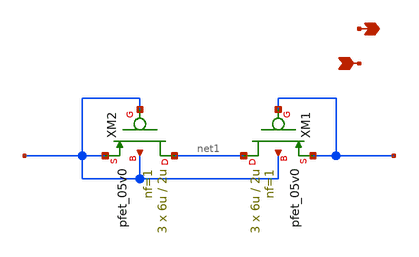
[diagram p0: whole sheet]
** sch_path: design/schematics/CCIA/CCIA/Resistors/NS_cic_bms_inst_amp_pseudo_res.sch
**.subckt NS_cic_bms_inst_amp_pseudo_res - +
*.opin -
*.ipin +
XM1 net1 - - + pfet_05v0 L=2u W=6u nf=1 ad='int((nf+1)/2) * W/nf * 0.18u' as='int((nf+2)/2) * W/nf * 0.18u'
+ pd='2*int((nf+1)/2) * (W/nf + 0.18u)' ps='2*int((nf+2)/2) * (W/nf + 0.18u)' nrd='0.18u / W' nrs='0.18u / W'
+ sa=0 sb=0 sd=0 m=3
XM2 net1 + + + pfet_05v0 L=2u W=6u nf=1 ad='int((nf+1)/2) * W/nf * 0.18u' as='int((nf+2)/2) * W/nf * 0.18u'
+ pd='2*int((nf+1)/2) * (W/nf + 0.18u)' ps='2*int((nf+2)/2) * (W/nf + 0.18u)' nrd='0.18u / W' nrs='0.18u / W'
+ sa=0 sb=0 sd=0 m=3
**.ends
.end
